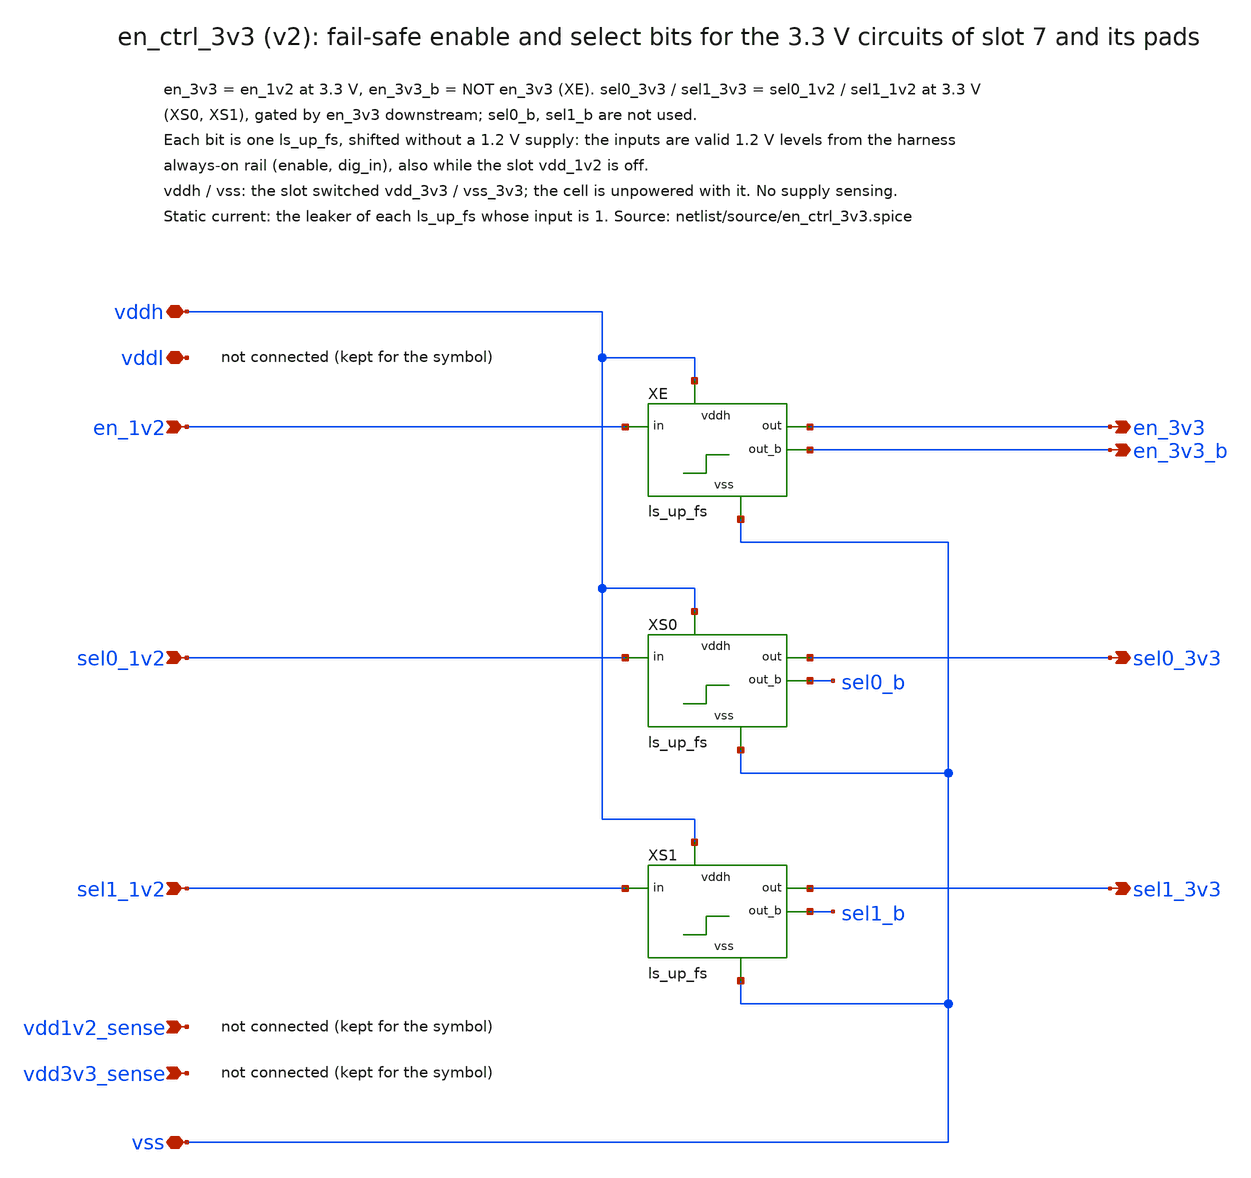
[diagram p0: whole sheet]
** sch_path: macros/en_ctrl_3v3/schematic/xschem/en_ctrl_3v3.sch
**.subckt en_ctrl_3v3 vddh vddl vss en_1v2 sel0_1v2 sel1_1v2 vdd1v2_sense vdd3v3_sense en_3v3
*+ sel0_3v3 sel1_3v3 en_3v3_b
*.iopin vddh
*.iopin vddl
*.iopin vss
*.ipin en_1v2
*.ipin sel0_1v2
*.ipin sel1_1v2
*.ipin vdd1v2_sense
*.ipin vdd3v3_sense
*.opin en_3v3
*.opin sel0_3v3
*.opin sel1_3v3
*.opin en_3v3_b
XE vddh vss en_1v2 en_3v3 en_3v3_b ls_up_fs
XS0 vddh vss sel0_1v2 sel0_3v3 sel0_b ls_up_fs
XS1 vddh vss sel1_1v2 sel1_3v3 sel1_b ls_up_fs
**.ends

* expanding   symbol:  ls_up_fs.sym # of pins=5
** sym_path: macros/en_ctrl_3v3/schematic/xschem/ls_up_fs.sym
** sch_path: macros/en_ctrl_3v3/schematic/xschem/ls_up_fs.sch
.subckt ls_up_fs vddh vss in out out_b
*.iopin vddh
*.iopin vss
*.ipin in
*.opin out
*.opin out_b
XN1 x in vss vss sg13_hv_nmos w=1u l=0.45u ng=1 m=1 mm_ok=1
XPL10 l9 in vddh vddh sg13_hv_pmos w=0.3u l=20u ng=1 m=1 mm_ok=1
XPL9 l8 in l9 vddh sg13_hv_pmos w=0.3u l=20u ng=1 m=1 mm_ok=1
XPL8 l7 in l8 vddh sg13_hv_pmos w=0.3u l=20u ng=1 m=1 mm_ok=1
XPL7 l6 in l7 vddh sg13_hv_pmos w=0.3u l=20u ng=1 m=1 mm_ok=1
XPL6 l5 in l6 vddh sg13_hv_pmos w=0.3u l=20u ng=1 m=1 mm_ok=1
XPL5 l4 in l5 vddh sg13_hv_pmos w=0.3u l=20u ng=1 m=1 mm_ok=1
XPL4 l3 in l4 vddh sg13_hv_pmos w=0.3u l=20u ng=1 m=1 mm_ok=1
XPL3 l2 in l3 vddh sg13_hv_pmos w=0.3u l=20u ng=1 m=1 mm_ok=1
XPL2 l1 in l2 vddh sg13_hv_pmos w=0.3u l=20u ng=1 m=1 mm_ok=1
XPL1 x in l1 vddh sg13_hv_pmos w=0.3u l=20u ng=1 m=1 mm_ok=1
XPF x y vddh vddh sg13_hv_pmos w=0.3u l=5u ng=1 m=1 mm_ok=1
XI1 vddh vss x y inv_hv
XI2 vddh vss y out_b inv_hv
XI3 vddh vss out_b out inv_hv
.ends


* expanding   symbol:  inv_hv.sym # of pins=4
** sym_path: macros/hv_logic/schematic/xschem/inv_hv.sym
** sch_path: macros/hv_logic/schematic/xschem/inv_hv.sch
.subckt inv_hv vdd vss a y
*.iopin vdd
*.iopin vss
*.ipin a
*.opin y
XP y a vdd vdd sg13_hv_pmos w=1u l=0.45u ng=1 m=1 mm_ok=1
XN y a vss vss sg13_hv_nmos w=1u l=0.45u ng=1 m=1 mm_ok=1
.ends

.end
